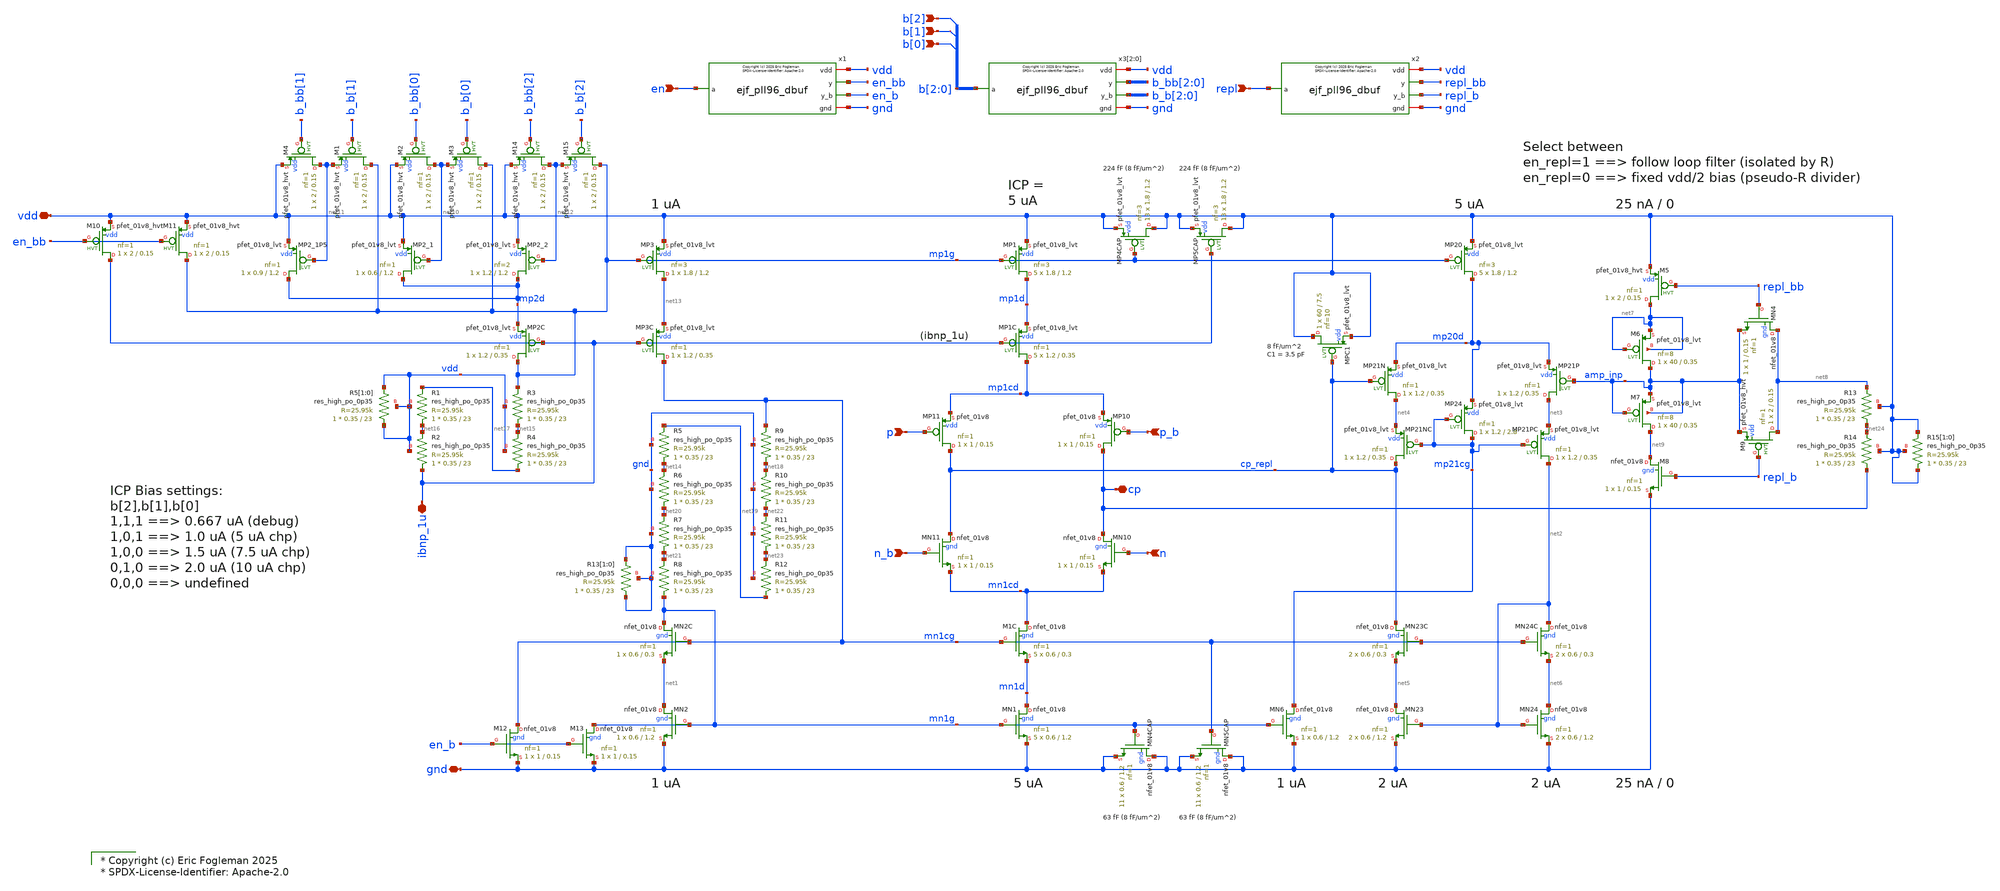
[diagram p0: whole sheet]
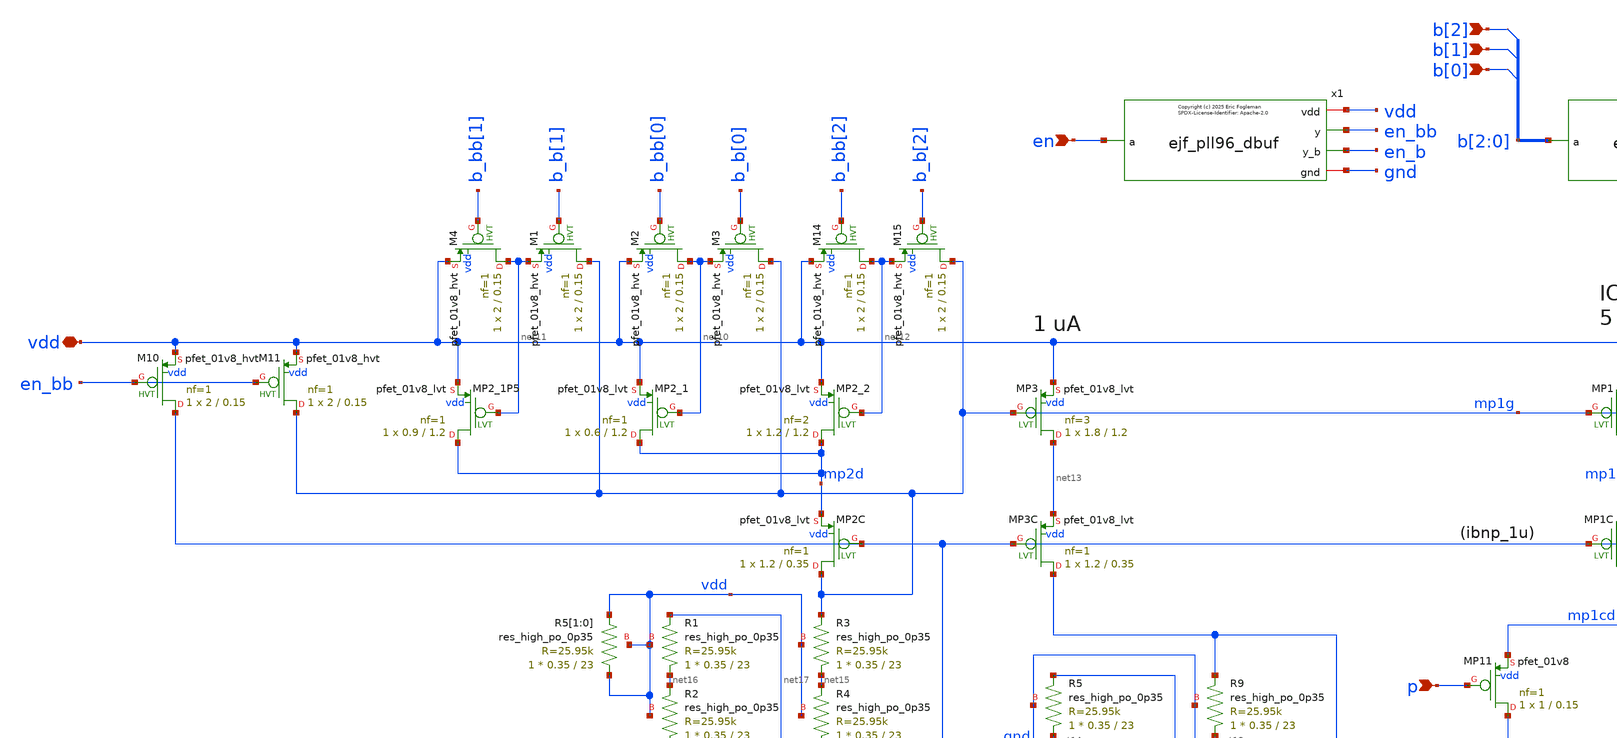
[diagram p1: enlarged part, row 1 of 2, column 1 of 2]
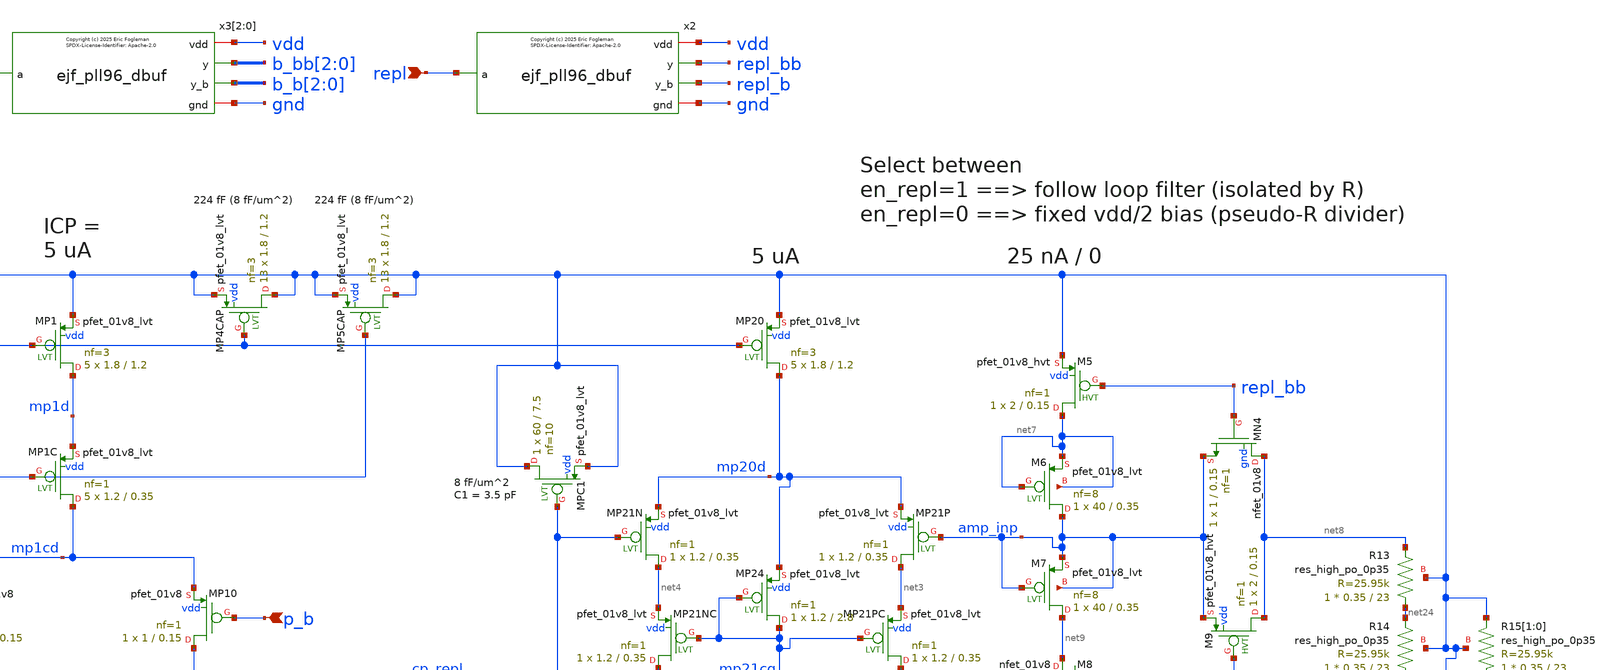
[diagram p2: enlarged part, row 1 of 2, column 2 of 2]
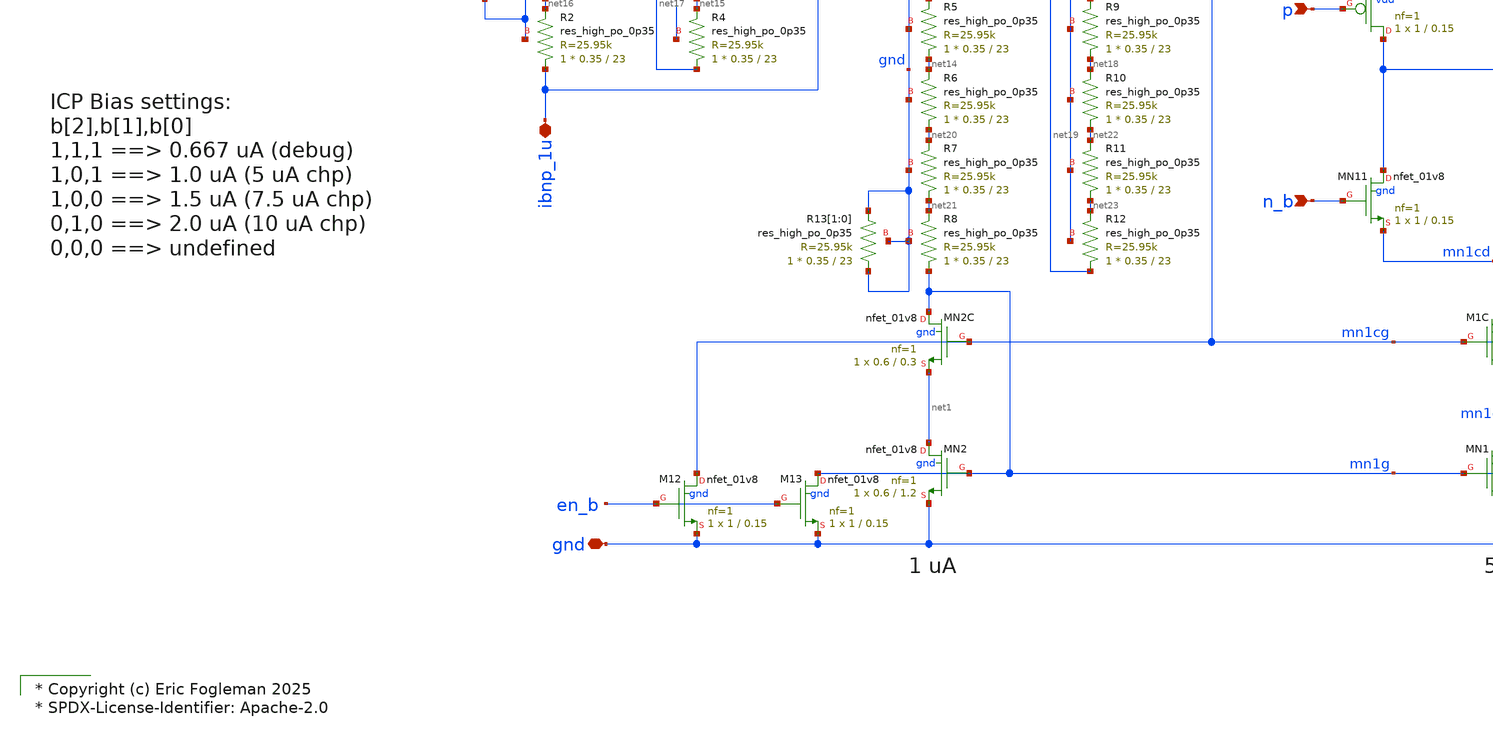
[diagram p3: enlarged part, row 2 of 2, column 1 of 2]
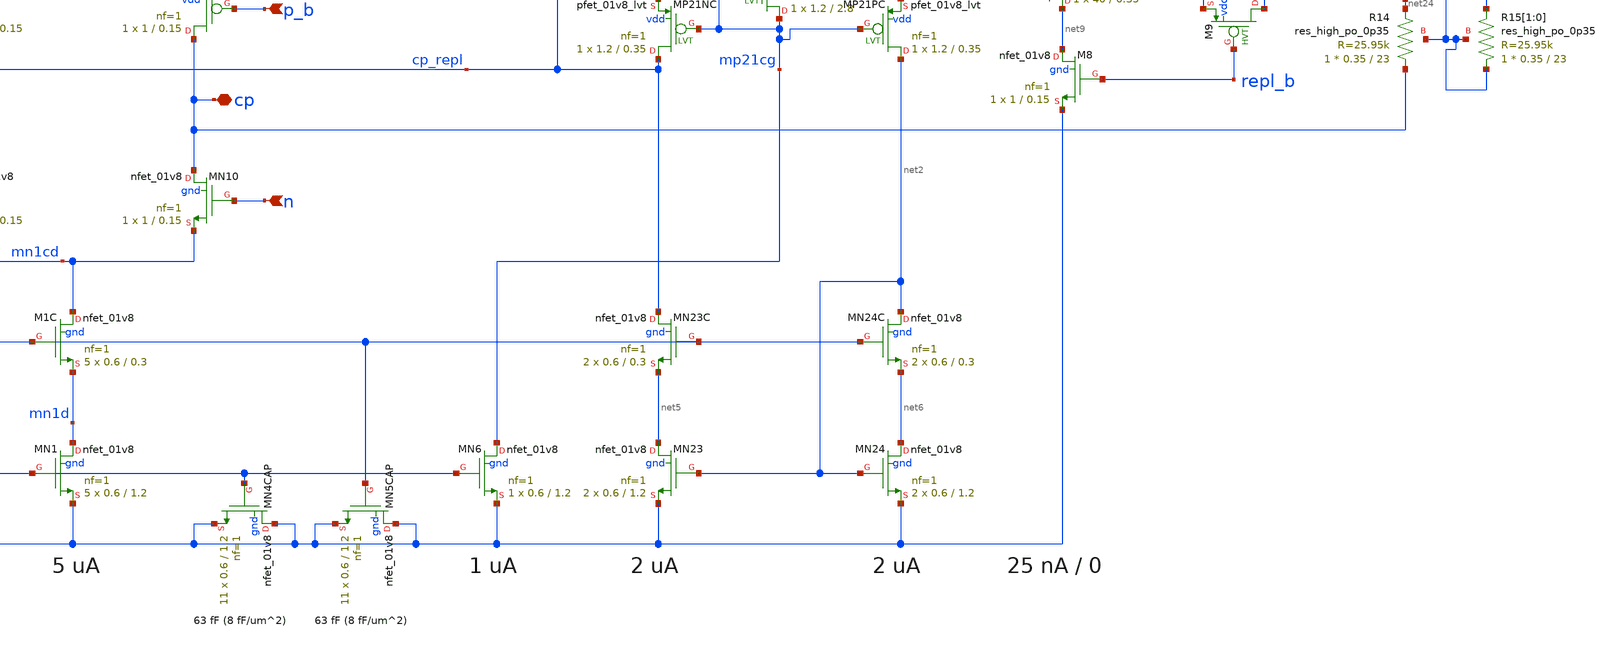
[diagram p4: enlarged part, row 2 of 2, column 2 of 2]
** sch_path: xschem/ejf_pll96_chp.sch
* xschem/ejf_pll96_dbuf.sym:
* Copyright (c) 2025 Eric Fogleman

* Copyright (c) Eric Fogleman 2025
* SPDX-License-Identifier: Apache-2.0

**.subckt ejf_pll96_chp vdd gnd ibnp_1u cp p n_b p_b n en b[2] repl b[1] b[0]
*.iopin vdd
*.iopin gnd
*.iopin ibnp_1u
*.iopin cp
*.ipin p
*.ipin n_b
*.ipin p_b
*.ipin n
*.ipin en
*.ipin b[2]
*.ipin repl
*.ipin b[1]
*.ipin b[0]
XMP2_2 mp2d net12 vdd vdd sky130_fd_pr__pfet_01v8_lvt L=1.2 W=1.2 nf=2 ad='int((nf+1)/2) * W/nf * 0.29'
+ as='int((nf+2)/2) * W/nf * 0.29' pd='2*int((nf+1)/2) * (W/nf + 0.29)' ps='2*int((nf+2)/2) * (W/nf + 0.29)'
+ nrd='0.29 / W' nrs='0.29 / W' sa=0 sb=0 sd=0 mult=1 m=1
XMN2 net1 mn1g gnd gnd sky130_fd_pr__nfet_01v8 L=1.2 W=0.6 nf=1 ad='int((nf+1)/2) * W/nf * 0.29' as='int((nf+2)/2) * W/nf * 0.29'
+ pd='2*int((nf+1)/2) * (W/nf + 0.29)' ps='2*int((nf+2)/2) * (W/nf + 0.29)' nrd='0.29 / W' nrs='0.29 / W'
+ sa=0 sb=0 sd=0 mult=1 m=1
XMN2C mn1g mn1cg net1 gnd sky130_fd_pr__nfet_01v8 L=0.3 W=0.6 nf=1 ad='int((nf+1)/2) * W/nf * 0.29' as='int((nf+2)/2) * W/nf * 0.29'
+ pd='2*int((nf+1)/2) * (W/nf + 0.29)' ps='2*int((nf+2)/2) * (W/nf + 0.29)' nrd='0.29 / W' nrs='0.29 / W'
+ sa=0 sb=0 sd=0 mult=1 m=1
XMP1 mp1d mp1g vdd vdd sky130_fd_pr__pfet_01v8_lvt L=1.2 W=1.8 nf=3 ad='int((nf+1)/2) * W/nf * 0.29'
+ as='int((nf+2)/2) * W/nf * 0.29' pd='2*int((nf+1)/2) * (W/nf + 0.29)' ps='2*int((nf+2)/2) * (W/nf + 0.29)'
+ nrd='0.29 / W' nrs='0.29 / W' sa=0 sb=0 sd=0 mult=5 m=5
XMP2C mp1g ibnp_1u mp2d vdd sky130_fd_pr__pfet_01v8_lvt L=0.35 W=1.2 nf=1 ad='int((nf+1)/2) * W/nf * 0.29'
+ as='int((nf+2)/2) * W/nf * 0.29' pd='2*int((nf+1)/2) * (W/nf + 0.29)' ps='2*int((nf+2)/2) * (W/nf + 0.29)'
+ nrd='0.29 / W' nrs='0.29 / W' sa=0 sb=0 sd=0 mult=1 m=1
XMP1C mp1cd ibnp_1u mp1d vdd sky130_fd_pr__pfet_01v8_lvt L=0.35 W=1.2 nf=1 ad='int((nf+1)/2) * W/nf * 0.29'
+ as='int((nf+2)/2) * W/nf * 0.29' pd='2*int((nf+1)/2) * (W/nf + 0.29)' ps='2*int((nf+2)/2) * (W/nf + 0.29)'
+ nrd='0.29 / W' nrs='0.29 / W' sa=0 sb=0 sd=0 mult=5 m=5
XMN1 mn1d mn1g gnd gnd sky130_fd_pr__nfet_01v8 L=1.2 W=0.6 nf=1 ad='int((nf+1)/2) * W/nf * 0.29' as='int((nf+2)/2) * W/nf * 0.29'
+ pd='2*int((nf+1)/2) * (W/nf + 0.29)' ps='2*int((nf+2)/2) * (W/nf + 0.29)' nrd='0.29 / W' nrs='0.29 / W'
+ sa=0 sb=0 sd=0 mult=5 m=5
XM1C mn1cd mn1cg mn1d gnd sky130_fd_pr__nfet_01v8 L=0.3 W=0.6 nf=1 ad='int((nf+1)/2) * W/nf * 0.29' as='int((nf+2)/2) * W/nf * 0.29'
+ pd='2*int((nf+1)/2) * (W/nf + 0.29)' ps='2*int((nf+2)/2) * (W/nf + 0.29)' nrd='0.29 / W' nrs='0.29 / W'
+ sa=0 sb=0 sd=0 mult=5 m=5
XMP11 cp_repl p mp1cd vdd sky130_fd_pr__pfet_01v8 L=0.15 W=1 nf=1 ad='int((nf+1)/2) * W/nf * 0.29' as='int((nf+2)/2) * W/nf * 0.29'
+ pd='2*int((nf+1)/2) * (W/nf + 0.29)' ps='2*int((nf+2)/2) * (W/nf + 0.29)' nrd='0.29 / W' nrs='0.29 / W'
+ sa=0 sb=0 sd=0 mult=1 m=1
XMN11 cp_repl n_b mn1cd gnd sky130_fd_pr__nfet_01v8 L=0.15 W=1 nf=1 ad='int((nf+1)/2) * W/nf * 0.29'
+ as='int((nf+2)/2) * W/nf * 0.29' pd='2*int((nf+1)/2) * (W/nf + 0.29)' ps='2*int((nf+2)/2) * (W/nf + 0.29)'
+ nrd='0.29 / W' nrs='0.29 / W' sa=0 sb=0 sd=0 mult=1 m=1
XMP10 cp p_b mp1cd vdd sky130_fd_pr__pfet_01v8 L=0.15 W=1 nf=1 ad='int((nf+1)/2) * W/nf * 0.29' as='int((nf+2)/2) * W/nf * 0.29'
+ pd='2*int((nf+1)/2) * (W/nf + 0.29)' ps='2*int((nf+2)/2) * (W/nf + 0.29)' nrd='0.29 / W' nrs='0.29 / W'
+ sa=0 sb=0 sd=0 mult=1 m=1
XMN10 cp n mn1cd gnd sky130_fd_pr__nfet_01v8 L=0.15 W=1 nf=1 ad='int((nf+1)/2) * W/nf * 0.29' as='int((nf+2)/2) * W/nf * 0.29'
+ pd='2*int((nf+1)/2) * (W/nf + 0.29)' ps='2*int((nf+2)/2) * (W/nf + 0.29)' nrd='0.29 / W' nrs='0.29 / W'
+ sa=0 sb=0 sd=0 mult=1 m=1
XMN4CAP gnd mn1g gnd gnd sky130_fd_pr__nfet_01v8 L=1.2 W=0.6 nf=1 ad='int((nf+1)/2) * W/nf * 0.29' as='int((nf+2)/2) * W/nf * 0.29'
+ pd='2*int((nf+1)/2) * (W/nf + 0.29)' ps='2*int((nf+2)/2) * (W/nf + 0.29)' nrd='0.29 / W' nrs='0.29 / W'
+ sa=0 sb=0 sd=0 mult=11 m=11
XMP4CAP vdd mp1g vdd vdd sky130_fd_pr__pfet_01v8_lvt L=1.2 W=1.8 nf=3 ad='int((nf+1)/2) * W/nf * 0.29'
+ as='int((nf+2)/2) * W/nf * 0.29' pd='2*int((nf+1)/2) * (W/nf + 0.29)' ps='2*int((nf+2)/2) * (W/nf + 0.29)'
+ nrd='0.29 / W' nrs='0.29 / W' sa=0 sb=0 sd=0 mult=13 m=13
XMP5CAP vdd ibnp_1u vdd vdd sky130_fd_pr__pfet_01v8_lvt L=1.2 W=1.8 nf=3 ad='int((nf+1)/2) * W/nf * 0.29'
+ as='int((nf+2)/2) * W/nf * 0.29' pd='2*int((nf+1)/2) * (W/nf + 0.29)' ps='2*int((nf+2)/2) * (W/nf + 0.29)'
+ nrd='0.29 / W' nrs='0.29 / W' sa=0 sb=0 sd=0 mult=13 m=13
XMN5CAP gnd mn1cg gnd gnd sky130_fd_pr__nfet_01v8 L=1.2 W=0.6 nf=1 ad='int((nf+1)/2) * W/nf * 0.29' as='int((nf+2)/2) * W/nf * 0.29'
+ pd='2*int((nf+1)/2) * (W/nf + 0.29)' ps='2*int((nf+2)/2) * (W/nf + 0.29)' nrd='0.29 / W' nrs='0.29 / W'
+ sa=0 sb=0 sd=0 mult=11 m=11
XMP20 mp20d mp1g vdd vdd sky130_fd_pr__pfet_01v8_lvt L=1.2 W=1.8 nf=3 ad='int((nf+1)/2) * W/nf * 0.29'
+ as='int((nf+2)/2) * W/nf * 0.29' pd='2*int((nf+1)/2) * (W/nf + 0.29)' ps='2*int((nf+2)/2) * (W/nf + 0.29)'
+ nrd='0.29 / W' nrs='0.29 / W' sa=0 sb=0 sd=0 mult=5 m=5
XMN6 mp21cg mn1g gnd gnd sky130_fd_pr__nfet_01v8 L=1.2 W=0.6 nf=1 ad='int((nf+1)/2) * W/nf * 0.29' as='int((nf+2)/2) * W/nf * 0.29'
+ pd='2*int((nf+1)/2) * (W/nf + 0.29)' ps='2*int((nf+2)/2) * (W/nf + 0.29)' nrd='0.29 / W' nrs='0.29 / W'
+ sa=0 sb=0 sd=0 mult=1 m=1
XMPC1 vdd cp_repl vdd vdd sky130_fd_pr__pfet_01v8_lvt L=7.5 W=60 nf=10 ad='int((nf+1)/2) * W/nf * 0.29'
+ as='int((nf+2)/2) * W/nf * 0.29' pd='2*int((nf+1)/2) * (W/nf + 0.29)' ps='2*int((nf+2)/2) * (W/nf + 0.29)'
+ nrd='0.29 / W' nrs='0.29 / W' sa=0 sb=0 sd=0 mult=1 m=1
XM12 mn1cg en_b gnd gnd sky130_fd_pr__nfet_01v8 L=0.15 W=1 nf=1 ad='int((nf+1)/2) * W/nf * 0.29' as='int((nf+2)/2) * W/nf * 0.29'
+ pd='2*int((nf+1)/2) * (W/nf + 0.29)' ps='2*int((nf+2)/2) * (W/nf + 0.29)' nrd='0.29 / W' nrs='0.29 / W'
+ sa=0 sb=0 sd=0 mult=1 m=1
XM13 mn1g en_b gnd gnd sky130_fd_pr__nfet_01v8 L=0.15 W=1 nf=1 ad='int((nf+1)/2) * W/nf * 0.29' as='int((nf+2)/2) * W/nf * 0.29'
+ pd='2*int((nf+1)/2) * (W/nf + 0.29)' ps='2*int((nf+2)/2) * (W/nf + 0.29)' nrd='0.29 / W' nrs='0.29 / W'
+ sa=0 sb=0 sd=0 mult=1 m=1
XMP21P net3 amp_inp mp20d vdd sky130_fd_pr__pfet_01v8_lvt L=0.35 W=1.2 nf=1 ad='int((nf+1)/2) * W/nf * 0.29'
+ as='int((nf+2)/2) * W/nf * 0.29' pd='2*int((nf+1)/2) * (W/nf + 0.29)' ps='2*int((nf+2)/2) * (W/nf + 0.29)'
+ nrd='0.29 / W' nrs='0.29 / W' sa=0 sb=0 sd=0 mult=1 m=1
XMP21N net4 cp_repl mp20d vdd sky130_fd_pr__pfet_01v8_lvt L=0.35 W=1.2 nf=1 ad='int((nf+1)/2) * W/nf * 0.29'
+ as='int((nf+2)/2) * W/nf * 0.29' pd='2*int((nf+1)/2) * (W/nf + 0.29)' ps='2*int((nf+2)/2) * (W/nf + 0.29)'
+ nrd='0.29 / W' nrs='0.29 / W' sa=0 sb=0 sd=0 mult=1 m=1
XMP24 mp21cg mp21cg mp20d vdd sky130_fd_pr__pfet_01v8_lvt L=2.8 W=1.2 nf=1 ad='int((nf+1)/2) * W/nf * 0.29'
+ as='int((nf+2)/2) * W/nf * 0.29' pd='2*int((nf+1)/2) * (W/nf + 0.29)' ps='2*int((nf+2)/2) * (W/nf + 0.29)'
+ nrd='0.29 / W' nrs='0.29 / W' sa=0 sb=0 sd=0 mult=1 m=1
XMP21NC cp_repl mp21cg net4 vdd sky130_fd_pr__pfet_01v8_lvt L=0.35 W=1.2 nf=1 ad='int((nf+1)/2) * W/nf * 0.29'
+ as='int((nf+2)/2) * W/nf * 0.29' pd='2*int((nf+1)/2) * (W/nf + 0.29)' ps='2*int((nf+2)/2) * (W/nf + 0.29)'
+ nrd='0.29 / W' nrs='0.29 / W' sa=0 sb=0 sd=0 mult=1 m=1
XMP21PC net2 mp21cg net3 vdd sky130_fd_pr__pfet_01v8_lvt L=0.35 W=1.2 nf=1 ad='int((nf+1)/2) * W/nf * 0.29'
+ as='int((nf+2)/2) * W/nf * 0.29' pd='2*int((nf+1)/2) * (W/nf + 0.29)' ps='2*int((nf+2)/2) * (W/nf + 0.29)'
+ nrd='0.29 / W' nrs='0.29 / W' sa=0 sb=0 sd=0 mult=1 m=1
XMN24 net6 net2 gnd gnd sky130_fd_pr__nfet_01v8 L=1.2 W=0.6 nf=1 ad='int((nf+1)/2) * W/nf * 0.29' as='int((nf+2)/2) * W/nf * 0.29'
+ pd='2*int((nf+1)/2) * (W/nf + 0.29)' ps='2*int((nf+2)/2) * (W/nf + 0.29)' nrd='0.29 / W' nrs='0.29 / W'
+ sa=0 sb=0 sd=0 mult=2 m=2
XMN23 net5 net2 gnd gnd sky130_fd_pr__nfet_01v8 L=1.2 W=0.6 nf=1 ad='int((nf+1)/2) * W/nf * 0.29' as='int((nf+2)/2) * W/nf * 0.29'
+ pd='2*int((nf+1)/2) * (W/nf + 0.29)' ps='2*int((nf+2)/2) * (W/nf + 0.29)' nrd='0.29 / W' nrs='0.29 / W'
+ sa=0 sb=0 sd=0 mult=2 m=2
XMN24C net2 mn1cg net6 gnd sky130_fd_pr__nfet_01v8 L=0.3 W=0.6 nf=1 ad='int((nf+1)/2) * W/nf * 0.29'
+ as='int((nf+2)/2) * W/nf * 0.29' pd='2*int((nf+1)/2) * (W/nf + 0.29)' ps='2*int((nf+2)/2) * (W/nf + 0.29)'
+ nrd='0.29 / W' nrs='0.29 / W' sa=0 sb=0 sd=0 mult=2 m=2
XMN23C cp_repl mn1cg net5 gnd sky130_fd_pr__nfet_01v8 L=0.3 W=0.6 nf=1 ad='int((nf+1)/2) * W/nf * 0.29'
+ as='int((nf+2)/2) * W/nf * 0.29' pd='2*int((nf+1)/2) * (W/nf + 0.29)' ps='2*int((nf+2)/2) * (W/nf + 0.29)'
+ nrd='0.29 / W' nrs='0.29 / W' sa=0 sb=0 sd=0 mult=2 m=2
XM8 net9 repl_b gnd gnd sky130_fd_pr__nfet_01v8 L=0.15 W=1 nf=1 ad='int((nf+1)/2) * W/nf * 0.29' as='int((nf+2)/2) * W/nf * 0.29'
+ pd='2*int((nf+1)/2) * (W/nf + 0.29)' ps='2*int((nf+2)/2) * (W/nf + 0.29)' nrd='0.29 / W' nrs='0.29 / W'
+ sa=0 sb=0 sd=0 mult=1 m=1
XM5 net7 repl_bb vdd vdd sky130_fd_pr__pfet_01v8_hvt L=0.15 W=2 nf=1 ad='int((nf+1)/2) * W/nf * 0.29'
+ as='int((nf+2)/2) * W/nf * 0.29' pd='2*int((nf+1)/2) * (W/nf + 0.29)' ps='2*int((nf+2)/2) * (W/nf + 0.29)'
+ nrd='0.29 / W' nrs='0.29 / W' sa=0 sb=0 sd=0 mult=1 m=1
XM6 amp_inp net7 net7 net7 sky130_fd_pr__pfet_01v8_lvt L=0.35 W=40 nf=8 ad='int((nf+1)/2) * W/nf * 0.29'
+ as='int((nf+2)/2) * W/nf * 0.29' pd='2*int((nf+1)/2) * (W/nf + 0.29)' ps='2*int((nf+2)/2) * (W/nf + 0.29)'
+ nrd='0.29 / W' nrs='0.29 / W' sa=0 sb=0 sd=0 mult=1 m=1
XM7 net9 amp_inp amp_inp amp_inp sky130_fd_pr__pfet_01v8_lvt L=0.35 W=40 nf=8 ad='int((nf+1)/2) * W/nf * 0.29'
+ as='int((nf+2)/2) * W/nf * 0.29' pd='2*int((nf+1)/2) * (W/nf + 0.29)' ps='2*int((nf+2)/2) * (W/nf + 0.29)'
+ nrd='0.29 / W' nrs='0.29 / W' sa=0 sb=0 sd=0 mult=1 m=1
XMN4 net8 repl_bb amp_inp gnd sky130_fd_pr__nfet_01v8 L=0.15 W=1 nf=1 ad='int((nf+1)/2) * W/nf * 0.29'
+ as='int((nf+2)/2) * W/nf * 0.29' pd='2*int((nf+1)/2) * (W/nf + 0.29)' ps='2*int((nf+2)/2) * (W/nf + 0.29)'
+ nrd='0.29 / W' nrs='0.29 / W' sa=0 sb=0 sd=0 mult=1 m=1
XM9 net8 repl_b amp_inp vdd sky130_fd_pr__pfet_01v8_hvt L=0.15 W=2 nf=1 ad='int((nf+1)/2) * W/nf * 0.29'
+ as='int((nf+2)/2) * W/nf * 0.29' pd='2*int((nf+1)/2) * (W/nf + 0.29)' ps='2*int((nf+2)/2) * (W/nf + 0.29)'
+ nrd='0.29 / W' nrs='0.29 / W' sa=0 sb=0 sd=0 mult=1 m=1
XMP2_1 mp2d net10 vdd vdd sky130_fd_pr__pfet_01v8_lvt L=1.2 W=0.6 nf=1 ad='int((nf+1)/2) * W/nf * 0.29'
+ as='int((nf+2)/2) * W/nf * 0.29' pd='2*int((nf+1)/2) * (W/nf + 0.29)' ps='2*int((nf+2)/2) * (W/nf + 0.29)'
+ nrd='0.29 / W' nrs='0.29 / W' sa=0 sb=0 sd=0 mult=1 m=1
XMP2_1P5 mp2d net11 vdd vdd sky130_fd_pr__pfet_01v8_lvt L=1.2 W=0.9 nf=1 ad='int((nf+1)/2) * W/nf * 0.29'
+ as='int((nf+2)/2) * W/nf * 0.29' pd='2*int((nf+1)/2) * (W/nf + 0.29)' ps='2*int((nf+2)/2) * (W/nf + 0.29)'
+ nrd='0.29 / W' nrs='0.29 / W' sa=0 sb=0 sd=0 mult=1 m=1
XM4 net11 b_bb[1] vdd vdd sky130_fd_pr__pfet_01v8_hvt L=0.15 W=2 nf=1 ad='int((nf+1)/2) * W/nf * 0.29'
+ as='int((nf+2)/2) * W/nf * 0.29' pd='2*int((nf+1)/2) * (W/nf + 0.29)' ps='2*int((nf+2)/2) * (W/nf + 0.29)'
+ nrd='0.29 / W' nrs='0.29 / W' sa=0 sb=0 sd=0 mult=1 m=1
XMP3C mn1cg ibnp_1u net13 vdd sky130_fd_pr__pfet_01v8_lvt L=0.35 W=1.2 nf=1 ad='int((nf+1)/2) * W/nf * 0.29'
+ as='int((nf+2)/2) * W/nf * 0.29' pd='2*int((nf+1)/2) * (W/nf + 0.29)' ps='2*int((nf+2)/2) * (W/nf + 0.29)'
+ nrd='0.29 / W' nrs='0.29 / W' sa=0 sb=0 sd=0 mult=1 m=1
XMP3 net13 mp1g vdd vdd sky130_fd_pr__pfet_01v8_lvt L=1.2 W=1.8 nf=3 ad='int((nf+1)/2) * W/nf * 0.29'
+ as='int((nf+2)/2) * W/nf * 0.29' pd='2*int((nf+1)/2) * (W/nf + 0.29)' ps='2*int((nf+2)/2) * (W/nf + 0.29)'
+ nrd='0.29 / W' nrs='0.29 / W' sa=0 sb=0 sd=0 mult=1 m=1
x1 vdd en en_bb en_b gnd ejf_pll96_dbuf
x2 vdd repl repl_bb repl_b gnd ejf_pll96_dbuf
x3[2] vdd b[2] b_bb[2] b_b[2] gnd ejf_pll96_dbuf
x3[1] vdd b[1] b_bb[1] b_b[1] gnd ejf_pll96_dbuf
x3[0] vdd b[0] b_bb[0] b_b[0] gnd ejf_pll96_dbuf
XM1 mp1g b_b[1] net11 vdd sky130_fd_pr__pfet_01v8_hvt L=0.15 W=2 nf=1 ad='int((nf+1)/2) * W/nf * 0.29'
+ as='int((nf+2)/2) * W/nf * 0.29' pd='2*int((nf+1)/2) * (W/nf + 0.29)' ps='2*int((nf+2)/2) * (W/nf + 0.29)'
+ nrd='0.29 / W' nrs='0.29 / W' sa=0 sb=0 sd=0 mult=1 m=1
XM2 net10 b_bb[0] vdd vdd sky130_fd_pr__pfet_01v8_hvt L=0.15 W=2 nf=1 ad='int((nf+1)/2) * W/nf * 0.29'
+ as='int((nf+2)/2) * W/nf * 0.29' pd='2*int((nf+1)/2) * (W/nf + 0.29)' ps='2*int((nf+2)/2) * (W/nf + 0.29)'
+ nrd='0.29 / W' nrs='0.29 / W' sa=0 sb=0 sd=0 mult=1 m=1
XM3 mp1g b_b[0] net10 vdd sky130_fd_pr__pfet_01v8_hvt L=0.15 W=2 nf=1 ad='int((nf+1)/2) * W/nf * 0.29'
+ as='int((nf+2)/2) * W/nf * 0.29' pd='2*int((nf+1)/2) * (W/nf + 0.29)' ps='2*int((nf+2)/2) * (W/nf + 0.29)'
+ nrd='0.29 / W' nrs='0.29 / W' sa=0 sb=0 sd=0 mult=1 m=1
XM10 ibnp_1u en_bb vdd vdd sky130_fd_pr__pfet_01v8_hvt L=0.15 W=2 nf=1 ad='int((nf+1)/2) * W/nf * 0.29'
+ as='int((nf+2)/2) * W/nf * 0.29' pd='2*int((nf+1)/2) * (W/nf + 0.29)' ps='2*int((nf+2)/2) * (W/nf + 0.29)'
+ nrd='0.29 / W' nrs='0.29 / W' sa=0 sb=0 sd=0 mult=1 m=1
XM11 mp1g en_bb vdd vdd sky130_fd_pr__pfet_01v8_hvt L=0.15 W=2 nf=1 ad='int((nf+1)/2) * W/nf * 0.29'
+ as='int((nf+2)/2) * W/nf * 0.29' pd='2*int((nf+1)/2) * (W/nf + 0.29)' ps='2*int((nf+2)/2) * (W/nf + 0.29)'
+ nrd='0.29 / W' nrs='0.29 / W' sa=0 sb=0 sd=0 mult=1 m=1
XR1 net16 net17 vdd sky130_fd_pr__res_high_po_0p35 L=23 mult=1 m=1
XR2 ibnp_1u net16 vdd sky130_fd_pr__res_high_po_0p35 L=23 mult=1 m=1
XR3 net15 mp1g vdd sky130_fd_pr__res_high_po_0p35 L=23 mult=1 m=1
XR4 net17 net15 vdd sky130_fd_pr__res_high_po_0p35 L=23 mult=1 m=1
XR5[1] vdd vdd vdd sky130_fd_pr__res_high_po_0p35 L=23 mult=1 m=1
XR5[0] vdd vdd vdd sky130_fd_pr__res_high_po_0p35 L=23 mult=1 m=1
XR5 net14 net19 gnd sky130_fd_pr__res_high_po_0p35 L=23 mult=1 m=1
XR6 net20 net14 gnd sky130_fd_pr__res_high_po_0p35 L=23 mult=1 m=1
XR7 net21 net20 gnd sky130_fd_pr__res_high_po_0p35 L=23 mult=1 m=1
XR8 mn1g net21 gnd sky130_fd_pr__res_high_po_0p35 L=23 mult=1 m=1
XR9 net18 mn1cg gnd sky130_fd_pr__res_high_po_0p35 L=23 mult=1 m=1
XR10 net22 net18 gnd sky130_fd_pr__res_high_po_0p35 L=23 mult=1 m=1
XR11 net23 net22 gnd sky130_fd_pr__res_high_po_0p35 L=23 mult=1 m=1
XR12 net19 net23 gnd sky130_fd_pr__res_high_po_0p35 L=23 mult=1 m=1
XR13[1] gnd gnd gnd sky130_fd_pr__res_high_po_0p35 L=23 mult=1 m=1
XR13[0] gnd gnd gnd sky130_fd_pr__res_high_po_0p35 L=23 mult=1 m=1
XR13 net24 net8 vdd sky130_fd_pr__res_high_po_0p35 L=23 mult=1 m=1
XR14 cp net24 vdd sky130_fd_pr__res_high_po_0p35 L=23 mult=1 m=1
XR15[1] vdd vdd vdd sky130_fd_pr__res_high_po_0p35 L=23 mult=1 m=1
XR15[0] vdd vdd vdd sky130_fd_pr__res_high_po_0p35 L=23 mult=1 m=1
XM14 net12 b_bb[2] vdd vdd sky130_fd_pr__pfet_01v8_hvt L=0.15 W=2 nf=1 ad='int((nf+1)/2) * W/nf * 0.29'
+ as='int((nf+2)/2) * W/nf * 0.29' pd='2*int((nf+1)/2) * (W/nf + 0.29)' ps='2*int((nf+2)/2) * (W/nf + 0.29)'
+ nrd='0.29 / W' nrs='0.29 / W' sa=0 sb=0 sd=0 mult=1 m=1
XM15 mp1g b_b[2] net12 vdd sky130_fd_pr__pfet_01v8_hvt L=0.15 W=2 nf=1 ad='int((nf+1)/2) * W/nf * 0.29'
+ as='int((nf+2)/2) * W/nf * 0.29' pd='2*int((nf+1)/2) * (W/nf + 0.29)' ps='2*int((nf+2)/2) * (W/nf + 0.29)'
+ nrd='0.29 / W' nrs='0.29 / W' sa=0 sb=0 sd=0 mult=1 m=1
**.ends

* expanding   symbol:  ejf_pll96_dbuf.sym # of pins=5
** sym_path: xschem/ejf_pll96_dbuf.sym
** sch_path: xschem/ejf_pll96_dbuf.sch
.subckt ejf_pll96_dbuf vdd a y y_b gnd
*.ipin a
*.iopin vdd
*.iopin gnd
*.opin y
*.opin y_b
XMP1 y_b a vdd vdd sky130_fd_pr__pfet_01v8_hvt L=0.15 W=2 nf=1 ad='int((nf+1)/2) * W/nf * 0.29' as='int((nf+2)/2) * W/nf * 0.29'
+ pd='2*int((nf+1)/2) * (W/nf + 0.29)' ps='2*int((nf+2)/2) * (W/nf + 0.29)' nrd='0.29 / W' nrs='0.29 / W'
+ sa=0 sb=0 sd=0 mult=1 m=1
XMP3 y y_b vdd vdd sky130_fd_pr__pfet_01v8_hvt L=0.15 W=2 nf=1 ad='int((nf+1)/2) * W/nf * 0.29' as='int((nf+2)/2) * W/nf * 0.29'
+ pd='2*int((nf+1)/2) * (W/nf + 0.29)' ps='2*int((nf+2)/2) * (W/nf + 0.29)' nrd='0.29 / W' nrs='0.29 / W'
+ sa=0 sb=0 sd=0 mult=1 m=1
XMN4 y y_b gnd gnd sky130_fd_pr__nfet_01v8 L=0.15 W=1 nf=1 ad='int((nf+1)/2) * W/nf * 0.29' as='int((nf+2)/2) * W/nf * 0.29'
+ pd='2*int((nf+1)/2) * (W/nf + 0.29)' ps='2*int((nf+2)/2) * (W/nf + 0.29)' nrd='0.29 / W' nrs='0.29 / W'
+ sa=0 sb=0 sd=0 mult=1 m=1
XMN2 y_b a gnd gnd sky130_fd_pr__nfet_01v8 L=0.15 W=1 nf=1 ad='int((nf+1)/2) * W/nf * 0.29' as='int((nf+2)/2) * W/nf * 0.29'
+ pd='2*int((nf+1)/2) * (W/nf + 0.29)' ps='2*int((nf+2)/2) * (W/nf + 0.29)' nrd='0.29 / W' nrs='0.29 / W'
+ sa=0 sb=0 sd=0 mult=1 m=1
**** begin user architecture code

* Copyright (c) Eric Fogleman 2025
* SPDX-License-Identifier: Apache-2.0

**** end user architecture code
.ends

.end
